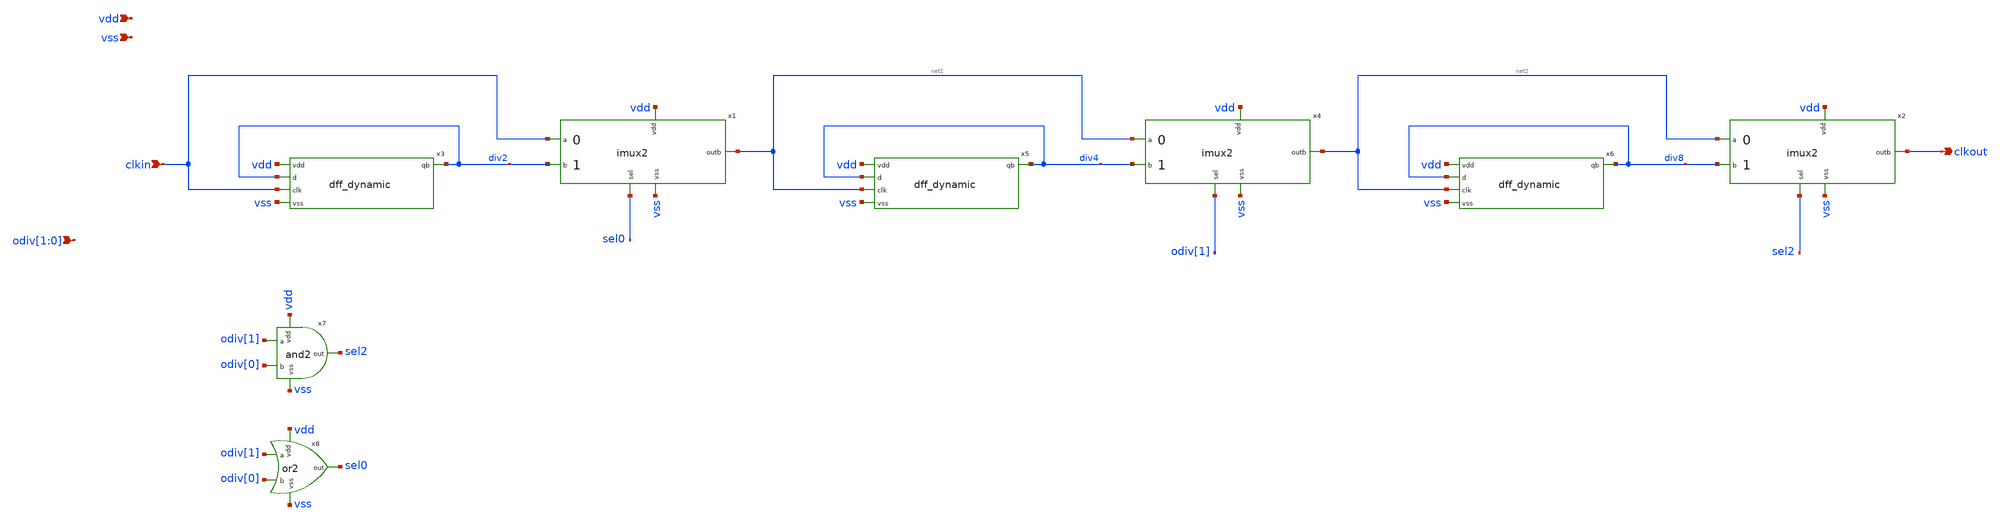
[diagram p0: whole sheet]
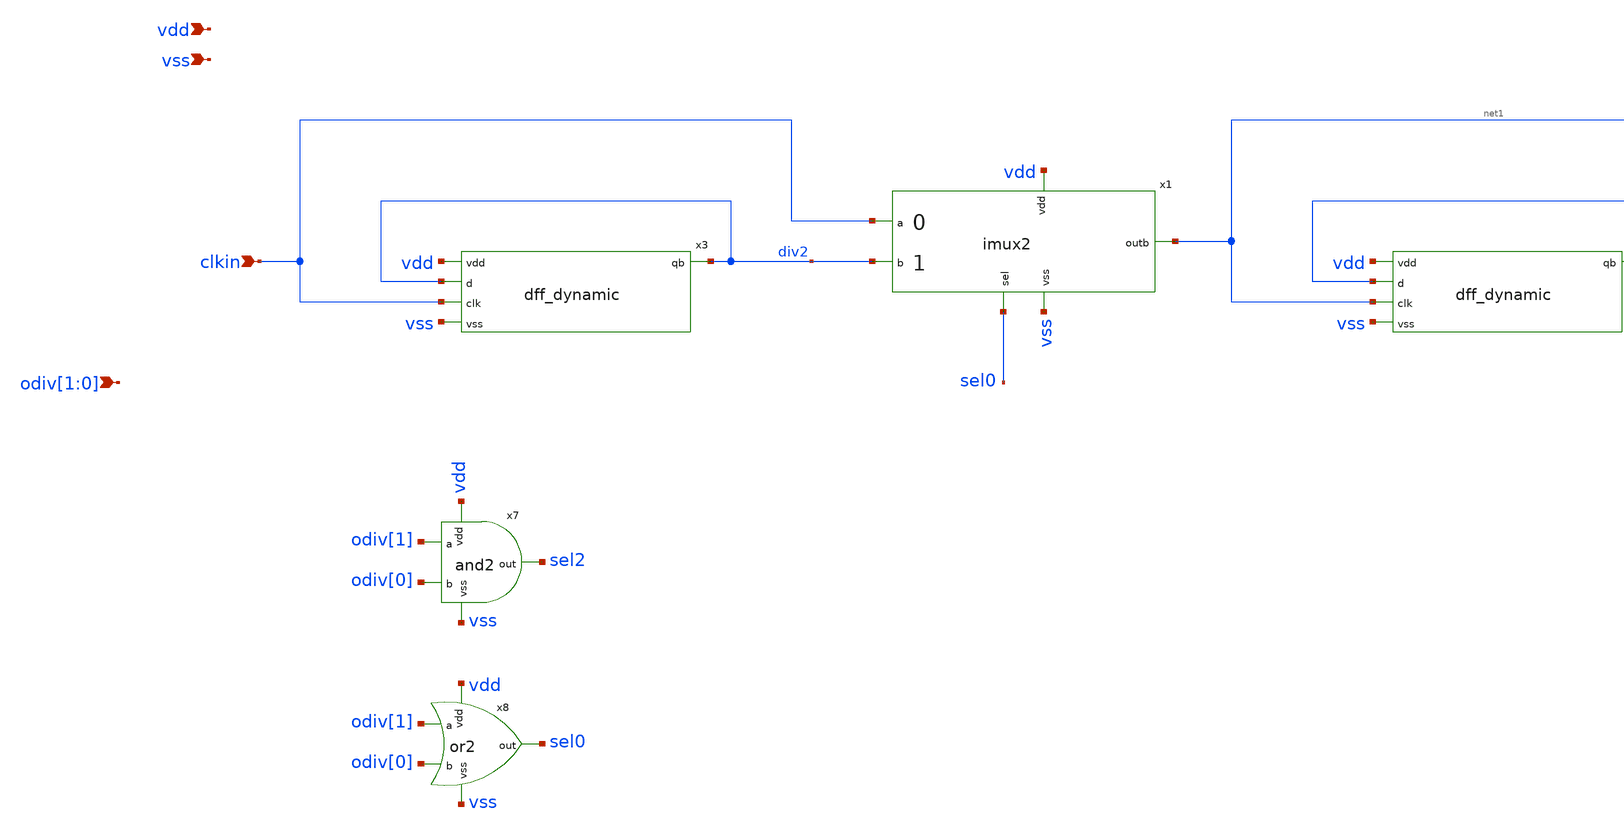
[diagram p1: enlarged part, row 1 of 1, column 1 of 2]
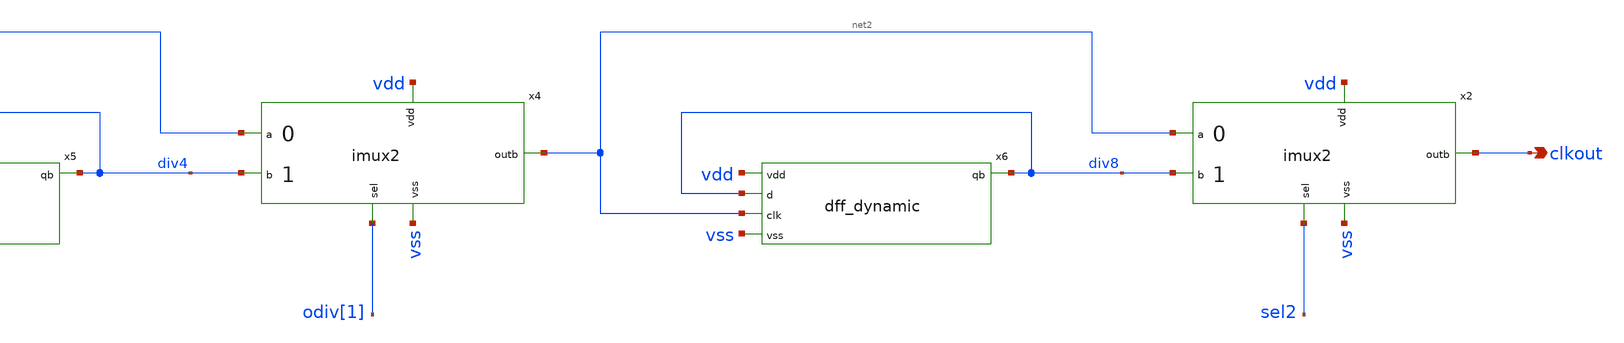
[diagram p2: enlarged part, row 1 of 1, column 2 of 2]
** sch_path: xschem/divout.sch
**.subckt divout odiv[1],odiv[0] clkin clkout vdd vss
*.ipin odiv[1],odiv[0]
*.ipin clkin
*.opin clkout
*.ipin vdd
*.ipin vss
x1 vdd sel0 div2 clkin net1 vss imux2
x3 div2 div2 vdd vss clkin dff_dynamic
x4 vdd odiv[1] div4 net1 net2 vss imux2
x5 div4 div4 vdd vss net1 dff_dynamic
x2 vdd sel2 div8 net2 clkout vss imux2
x6 div8 div8 vdd vss net2 dff_dynamic
x7 vdd odiv[1] odiv[0] sel2 vss and2
x8 vdd odiv[1] odiv[0] sel0 vss or2
**.ends

* expanding   symbol:  imux2.sym # of pins=6
** sym_path: xschem/imux2.sym
** sch_path: xschem/imux2.sch
.subckt imux2 vdd sel b a outb vss
*.ipin b
*.ipin a
*.ipin sel
*.ipin vdd
*.ipin vss
*.opin outb
XM1 net2 b vdd vdd pfet_03v3 L=0.28u W=8u nf=1 ad='int((nf+1)/2) * W/nf * 0.18u' as='int((nf+2)/2) * W/nf * 0.18u'
+ pd='2*int((nf+1)/2) * (W/nf + 0.18u)' ps='2*int((nf+2)/2) * (W/nf + 0.18u)' nrd='0.18u / W' nrs='0.18u / W'
+ sa=0 sb=0 sd=0 m=1
XM2 net1 b vss vss nfet_03v3 L=0.28u W=4u nf=1 ad='int((nf+1)/2) * W/nf * 0.18u' as='int((nf+2)/2) * W/nf * 0.18u'
+ pd='2*int((nf+1)/2) * (W/nf + 0.18u)' ps='2*int((nf+2)/2) * (W/nf + 0.18u)' nrd='0.18u / W' nrs='0.18u / W'
+ sa=0 sb=0 sd=0 m=1
XM3 outb sel net1 vss nfet_03v3 L=0.28u W=4u nf=1 ad='int((nf+1)/2) * W/nf * 0.18u' as='int((nf+2)/2) * W/nf * 0.18u'
+ pd='2*int((nf+1)/2) * (W/nf + 0.18u)' ps='2*int((nf+2)/2) * (W/nf + 0.18u)' nrd='0.18u / W' nrs='0.18u / W'
+ sa=0 sb=0 sd=0 m=1
XM4 outb selb net2 vdd pfet_03v3 L=0.28u W=8u nf=1 ad='int((nf+1)/2) * W/nf * 0.18u' as='int((nf+2)/2) * W/nf * 0.18u'
+ pd='2*int((nf+1)/2) * (W/nf + 0.18u)' ps='2*int((nf+2)/2) * (W/nf + 0.18u)' nrd='0.18u / W' nrs='0.18u / W'
+ sa=0 sb=0 sd=0 m=1
XM5 net4 a vdd vdd pfet_03v3 L=0.28u W=8u nf=1 ad='int((nf+1)/2) * W/nf * 0.18u' as='int((nf+2)/2) * W/nf * 0.18u'
+ pd='2*int((nf+1)/2) * (W/nf + 0.18u)' ps='2*int((nf+2)/2) * (W/nf + 0.18u)' nrd='0.18u / W' nrs='0.18u / W'
+ sa=0 sb=0 sd=0 m=1
XM6 net3 a vss vss nfet_03v3 L=0.28u W=4u nf=1 ad='int((nf+1)/2) * W/nf * 0.18u' as='int((nf+2)/2) * W/nf * 0.18u'
+ pd='2*int((nf+1)/2) * (W/nf + 0.18u)' ps='2*int((nf+2)/2) * (W/nf + 0.18u)' nrd='0.18u / W' nrs='0.18u / W'
+ sa=0 sb=0 sd=0 m=1
XM7 outb selb net3 vss nfet_03v3 L=0.28u W=4u nf=1 ad='int((nf+1)/2) * W/nf * 0.18u' as='int((nf+2)/2) * W/nf * 0.18u'
+ pd='2*int((nf+1)/2) * (W/nf + 0.18u)' ps='2*int((nf+2)/2) * (W/nf + 0.18u)' nrd='0.18u / W' nrs='0.18u / W'
+ sa=0 sb=0 sd=0 m=1
XM8 outb sel net4 vdd pfet_03v3 L=0.28u W=8u nf=1 ad='int((nf+1)/2) * W/nf * 0.18u' as='int((nf+2)/2) * W/nf * 0.18u'
+ pd='2*int((nf+1)/2) * (W/nf + 0.18u)' ps='2*int((nf+2)/2) * (W/nf + 0.18u)' nrd='0.18u / W' nrs='0.18u / W'
+ sa=0 sb=0 sd=0 m=1
XM9 selb sel vdd vdd pfet_03v3 L=0.28u W=8u nf=1 ad='int((nf+1)/2) * W/nf * 0.18u' as='int((nf+2)/2) * W/nf * 0.18u'
+ pd='2*int((nf+1)/2) * (W/nf + 0.18u)' ps='2*int((nf+2)/2) * (W/nf + 0.18u)' nrd='0.18u / W' nrs='0.18u / W'
+ sa=0 sb=0 sd=0 m=1
XM10 selb sel vss vss nfet_03v3 L=0.28u W=4u nf=1 ad='int((nf+1)/2) * W/nf * 0.18u' as='int((nf+2)/2) * W/nf * 0.18u'
+ pd='2*int((nf+1)/2) * (W/nf + 0.18u)' ps='2*int((nf+2)/2) * (W/nf + 0.18u)' nrd='0.18u / W' nrs='0.18u / W'
+ sa=0 sb=0 sd=0 m=1
.ends


* expanding   symbol:  dff_dynamic.sym # of pins=5
** sym_path: xschem/dff_dynamic.sym
** sch_path: xschem/dff_dynamic.sch
.subckt dff_dynamic qb d vdd vss clk
*.ipin d
*.ipin vdd
*.ipin vss
*.ipin clk
*.opin qb
XM1 net1 d vss vss nfet_03v3 L=0.28u W=1u nf=1 ad='int((nf+1)/2) * W/nf * 0.18u' as='int((nf+2)/2) * W/nf * 0.18u'
+ pd='2*int((nf+1)/2) * (W/nf + 0.18u)' ps='2*int((nf+2)/2) * (W/nf + 0.18u)' nrd='0.18u / W' nrs='0.18u / W'
+ sa=0 sb=0 sd=0 m=1
XM2 net1 d vdd vdd pfet_03v3 L=0.28u W=2u nf=1 ad='int((nf+1)/2) * W/nf * 0.18u' as='int((nf+2)/2) * W/nf * 0.18u'
+ pd='2*int((nf+1)/2) * (W/nf + 0.18u)' ps='2*int((nf+2)/2) * (W/nf + 0.18u)' nrd='0.18u / W' nrs='0.18u / W'
+ sa=0 sb=0 sd=0 m=1
XM3 net1 clkb net2 vss nfet_03v3 L=0.28u W=1u nf=1 ad='int((nf+1)/2) * W/nf * 0.18u' as='int((nf+2)/2) * W/nf * 0.18u'
+ pd='2*int((nf+1)/2) * (W/nf + 0.18u)' ps='2*int((nf+2)/2) * (W/nf + 0.18u)' nrd='0.18u / W' nrs='0.18u / W'
+ sa=0 sb=0 sd=0 m=1
XM4 net1 clk net2 vdd pfet_03v3 L=0.28u W=2u nf=1 ad='int((nf+1)/2) * W/nf * 0.18u' as='int((nf+2)/2) * W/nf * 0.18u'
+ pd='2*int((nf+1)/2) * (W/nf + 0.18u)' ps='2*int((nf+2)/2) * (W/nf + 0.18u)' nrd='0.18u / W' nrs='0.18u / W'
+ sa=0 sb=0 sd=0 m=1
XM5 net3 net2 vss vss nfet_03v3 L=0.28u W=1u nf=1 ad='int((nf+1)/2) * W/nf * 0.18u' as='int((nf+2)/2) * W/nf * 0.18u'
+ pd='2*int((nf+1)/2) * (W/nf + 0.18u)' ps='2*int((nf+2)/2) * (W/nf + 0.18u)' nrd='0.18u / W' nrs='0.18u / W'
+ sa=0 sb=0 sd=0 m=1
XM6 net3 net2 vdd vdd pfet_03v3 L=0.28u W=2u nf=1 ad='int((nf+1)/2) * W/nf * 0.18u' as='int((nf+2)/2) * W/nf * 0.18u'
+ pd='2*int((nf+1)/2) * (W/nf + 0.18u)' ps='2*int((nf+2)/2) * (W/nf + 0.18u)' nrd='0.18u / W' nrs='0.18u / W'
+ sa=0 sb=0 sd=0 m=1
XM7 net4 clk net3 vss nfet_03v3 L=0.28u W=1u nf=1 ad='int((nf+1)/2) * W/nf * 0.18u' as='int((nf+2)/2) * W/nf * 0.18u'
+ pd='2*int((nf+1)/2) * (W/nf + 0.18u)' ps='2*int((nf+2)/2) * (W/nf + 0.18u)' nrd='0.18u / W' nrs='0.18u / W'
+ sa=0 sb=0 sd=0 m=1
XM8 net4 clkb net3 vdd pfet_03v3 L=0.28u W=2u nf=1 ad='int((nf+1)/2) * W/nf * 0.18u' as='int((nf+2)/2) * W/nf * 0.18u'
+ pd='2*int((nf+1)/2) * (W/nf + 0.18u)' ps='2*int((nf+2)/2) * (W/nf + 0.18u)' nrd='0.18u / W' nrs='0.18u / W'
+ sa=0 sb=0 sd=0 m=1
XM9 qb net4 vss vss nfet_03v3 L=0.28u W=1u nf=1 ad='int((nf+1)/2) * W/nf * 0.18u' as='int((nf+2)/2) * W/nf * 0.18u'
+ pd='2*int((nf+1)/2) * (W/nf + 0.18u)' ps='2*int((nf+2)/2) * (W/nf + 0.18u)' nrd='0.18u / W' nrs='0.18u / W'
+ sa=0 sb=0 sd=0 m=1
XM10 qb net4 vdd vdd pfet_03v3 L=0.28u W=2u nf=1 ad='int((nf+1)/2) * W/nf * 0.18u' as='int((nf+2)/2) * W/nf * 0.18u'
+ pd='2*int((nf+1)/2) * (W/nf + 0.18u)' ps='2*int((nf+2)/2) * (W/nf + 0.18u)' nrd='0.18u / W' nrs='0.18u / W'
+ sa=0 sb=0 sd=0 m=1
XM11 clkb clk vss vss nfet_03v3 L=0.28u W=1u nf=1 ad='int((nf+1)/2) * W/nf * 0.18u' as='int((nf+2)/2) * W/nf * 0.18u'
+ pd='2*int((nf+1)/2) * (W/nf + 0.18u)' ps='2*int((nf+2)/2) * (W/nf + 0.18u)' nrd='0.18u / W' nrs='0.18u / W'
+ sa=0 sb=0 sd=0 m=1
XM12 clkb clk vdd vdd pfet_03v3 L=0.28u W=2u nf=1 ad='int((nf+1)/2) * W/nf * 0.18u' as='int((nf+2)/2) * W/nf * 0.18u'
+ pd='2*int((nf+1)/2) * (W/nf + 0.18u)' ps='2*int((nf+2)/2) * (W/nf + 0.18u)' nrd='0.18u / W' nrs='0.18u / W'
+ sa=0 sb=0 sd=0 m=1
.ends


* expanding   symbol:  and2.sym # of pins=5
** sym_path: xschem/and2.sym
** sch_path: xschem/and2.sch
.subckt and2 vdd a b out vss
*.ipin a
*.ipin b
*.ipin vdd
*.ipin vss
*.opin out
XM47 net1 b net2 vss nfet_03v3 L=0.28u W=0.6u nf=1 ad='int((nf+1)/2) * W/nf * 0.18u' as='int((nf+2)/2) * W/nf * 0.18u'
+ pd='2*int((nf+1)/2) * (W/nf + 0.18u)' ps='2*int((nf+2)/2) * (W/nf + 0.18u)' nrd='0.18u / W' nrs='0.18u / W'
+ sa=0 sb=0 sd=0 m=1
XM48 net1 b vdd vdd pfet_03v3 L=0.28u W=1.2u nf=1 ad='int((nf+1)/2) * W/nf * 0.18u' as='int((nf+2)/2) * W/nf * 0.18u'
+ pd='2*int((nf+1)/2) * (W/nf + 0.18u)' ps='2*int((nf+2)/2) * (W/nf + 0.18u)' nrd='0.18u / W' nrs='0.18u / W'
+ sa=0 sb=0 sd=0 m=1
XM49 net2 a vss vss nfet_03v3 L=0.28u W=0.6u nf=1 ad='int((nf+1)/2) * W/nf * 0.18u' as='int((nf+2)/2) * W/nf * 0.18u'
+ pd='2*int((nf+1)/2) * (W/nf + 0.18u)' ps='2*int((nf+2)/2) * (W/nf + 0.18u)' nrd='0.18u / W' nrs='0.18u / W'
+ sa=0 sb=0 sd=0 m=1
XM50 net1 a vdd vdd pfet_03v3 L=0.28u W=1.2u nf=1 ad='int((nf+1)/2) * W/nf * 0.18u' as='int((nf+2)/2) * W/nf * 0.18u'
+ pd='2*int((nf+1)/2) * (W/nf + 0.18u)' ps='2*int((nf+2)/2) * (W/nf + 0.18u)' nrd='0.18u / W' nrs='0.18u / W'
+ sa=0 sb=0 sd=0 m=1
XM51 out net1 vss vss nfet_03v3 L=0.28u W=0.6u nf=1 ad='int((nf+1)/2) * W/nf * 0.18u' as='int((nf+2)/2) * W/nf * 0.18u'
+ pd='2*int((nf+1)/2) * (W/nf + 0.18u)' ps='2*int((nf+2)/2) * (W/nf + 0.18u)' nrd='0.18u / W' nrs='0.18u / W'
+ sa=0 sb=0 sd=0 m=1
XM52 out net1 vdd vdd pfet_03v3 L=0.28u W=1.2u nf=1 ad='int((nf+1)/2) * W/nf * 0.18u' as='int((nf+2)/2) * W/nf * 0.18u'
+ pd='2*int((nf+1)/2) * (W/nf + 0.18u)' ps='2*int((nf+2)/2) * (W/nf + 0.18u)' nrd='0.18u / W' nrs='0.18u / W'
+ sa=0 sb=0 sd=0 m=1
.ends


* expanding   symbol:  or2.sym # of pins=5
** sym_path: xschem/or2.sym
** sch_path: xschem/or2.sch
.subckt or2 vdd a b out vss
*.ipin a
*.ipin b
*.ipin vdd
*.ipin vss
*.opin out
XM29 net1 b vss vss nfet_03v3 L=0.28u W=0.6u nf=1 ad='int((nf+1)/2) * W/nf * 0.18u' as='int((nf+2)/2) * W/nf * 0.18u'
+ pd='2*int((nf+1)/2) * (W/nf + 0.18u)' ps='2*int((nf+2)/2) * (W/nf + 0.18u)' nrd='0.18u / W' nrs='0.18u / W'
+ sa=0 sb=0 sd=0 m=1
XM30 net2 a vdd vdd pfet_03v3 L=0.28u W=1.2u nf=1 ad='int((nf+1)/2) * W/nf * 0.18u' as='int((nf+2)/2) * W/nf * 0.18u'
+ pd='2*int((nf+1)/2) * (W/nf + 0.18u)' ps='2*int((nf+2)/2) * (W/nf + 0.18u)' nrd='0.18u / W' nrs='0.18u / W'
+ sa=0 sb=0 sd=0 m=1
XM31 net1 a vss vss nfet_03v3 L=0.28u W=0.6u nf=1 ad='int((nf+1)/2) * W/nf * 0.18u' as='int((nf+2)/2) * W/nf * 0.18u'
+ pd='2*int((nf+1)/2) * (W/nf + 0.18u)' ps='2*int((nf+2)/2) * (W/nf + 0.18u)' nrd='0.18u / W' nrs='0.18u / W'
+ sa=0 sb=0 sd=0 m=1
XM32 net1 b net2 vdd pfet_03v3 L=0.28u W=1.2u nf=1 ad='int((nf+1)/2) * W/nf * 0.18u' as='int((nf+2)/2) * W/nf * 0.18u'
+ pd='2*int((nf+1)/2) * (W/nf + 0.18u)' ps='2*int((nf+2)/2) * (W/nf + 0.18u)' nrd='0.18u / W' nrs='0.18u / W'
+ sa=0 sb=0 sd=0 m=1
XM13 out net1 vss vss nfet_03v3 L=0.28u W=0.6u nf=1 ad='int((nf+1)/2) * W/nf * 0.18u' as='int((nf+2)/2) * W/nf * 0.18u'
+ pd='2*int((nf+1)/2) * (W/nf + 0.18u)' ps='2*int((nf+2)/2) * (W/nf + 0.18u)' nrd='0.18u / W' nrs='0.18u / W'
+ sa=0 sb=0 sd=0 m=1
XM14 out net1 vdd vdd pfet_03v3 L=0.28u W=1.2u nf=1 ad='int((nf+1)/2) * W/nf * 0.18u' as='int((nf+2)/2) * W/nf * 0.18u'
+ pd='2*int((nf+1)/2) * (W/nf + 0.18u)' ps='2*int((nf+2)/2) * (W/nf + 0.18u)' nrd='0.18u / W' nrs='0.18u / W'
+ sa=0 sb=0 sd=0 m=1
.ends

.end
